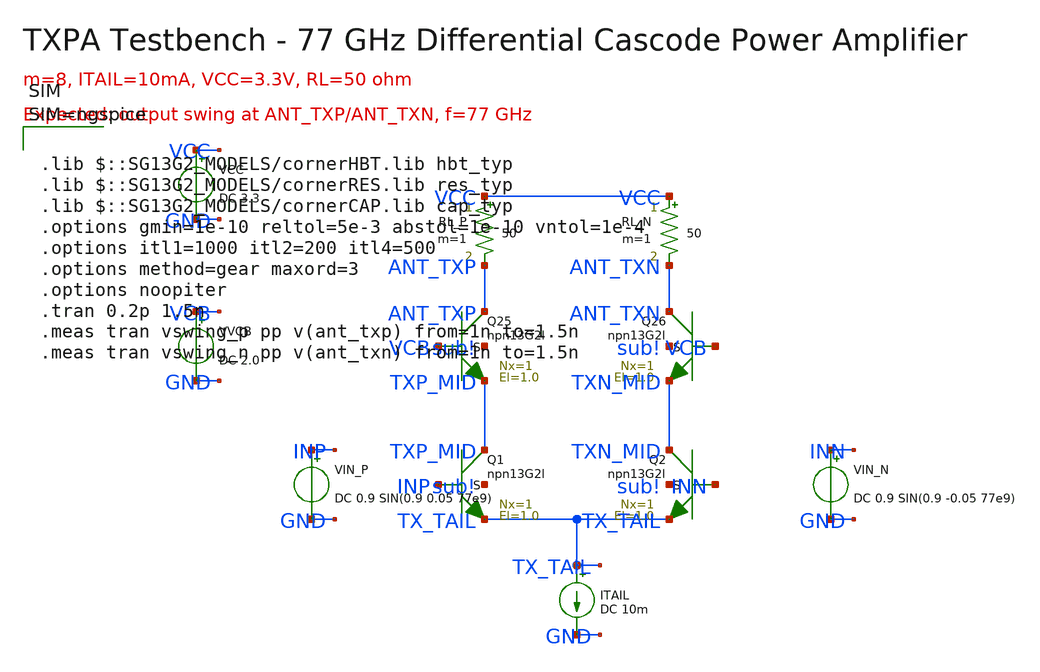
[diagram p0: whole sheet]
** sch_path: layout/testbenches/tb_txpa.sch
**.subckt tb_txpa
XQ1 TXP_MID INP TX_TAIL sub! npn13G2l Nx=1 El=1.0 mm_ok=1
XQ2 TXN_MID INN TX_TAIL sub! npn13G2l Nx=1 El=1.0 mm_ok=1
XQ25 ANT_TXP VCB TXP_MID sub! npn13G2l Nx=1 El=1.0 mm_ok=1
XQ26 ANT_TXN VCB TXN_MID sub! npn13G2l Nx=1 El=1.0 mm_ok=1
RL_P VCC ANT_TXP 50 m=1
RL_N VCC ANT_TXN 50 m=1
VCC VCC GND DC 3.3
ITAIL TX_TAIL GND DC 10m
VIN_P INP GND DC 0.9 SIN(0.9 0.05 77e9)
VIN_N INN GND DC 0.9 SIN(0.9 -0.05 77e9)
VVCB VCB GND DC 2.0
**** begin user architecture code



.lib $::SG13G2_MODELS/cornerHBT.lib hbt_typ
.lib $::SG13G2_MODELS/cornerRES.lib res_typ
.lib $::SG13G2_MODELS/cornerCAP.lib cap_typ
.options gmin=1e-10 reltol=5e-3 abstol=1e-10 vntol=1e-4
.options itl1=1000 itl2=200 itl4=500
.options method=gear maxord=3
.options noopiter
.tran 0.2p 1.5n
.meas tran vswing_p pp v(ant_txp) from=1n to=1.5n
.meas tran vswing_n pp v(ant_txn) from=1n to=1.5n



**** end user architecture code
**.ends
.end
